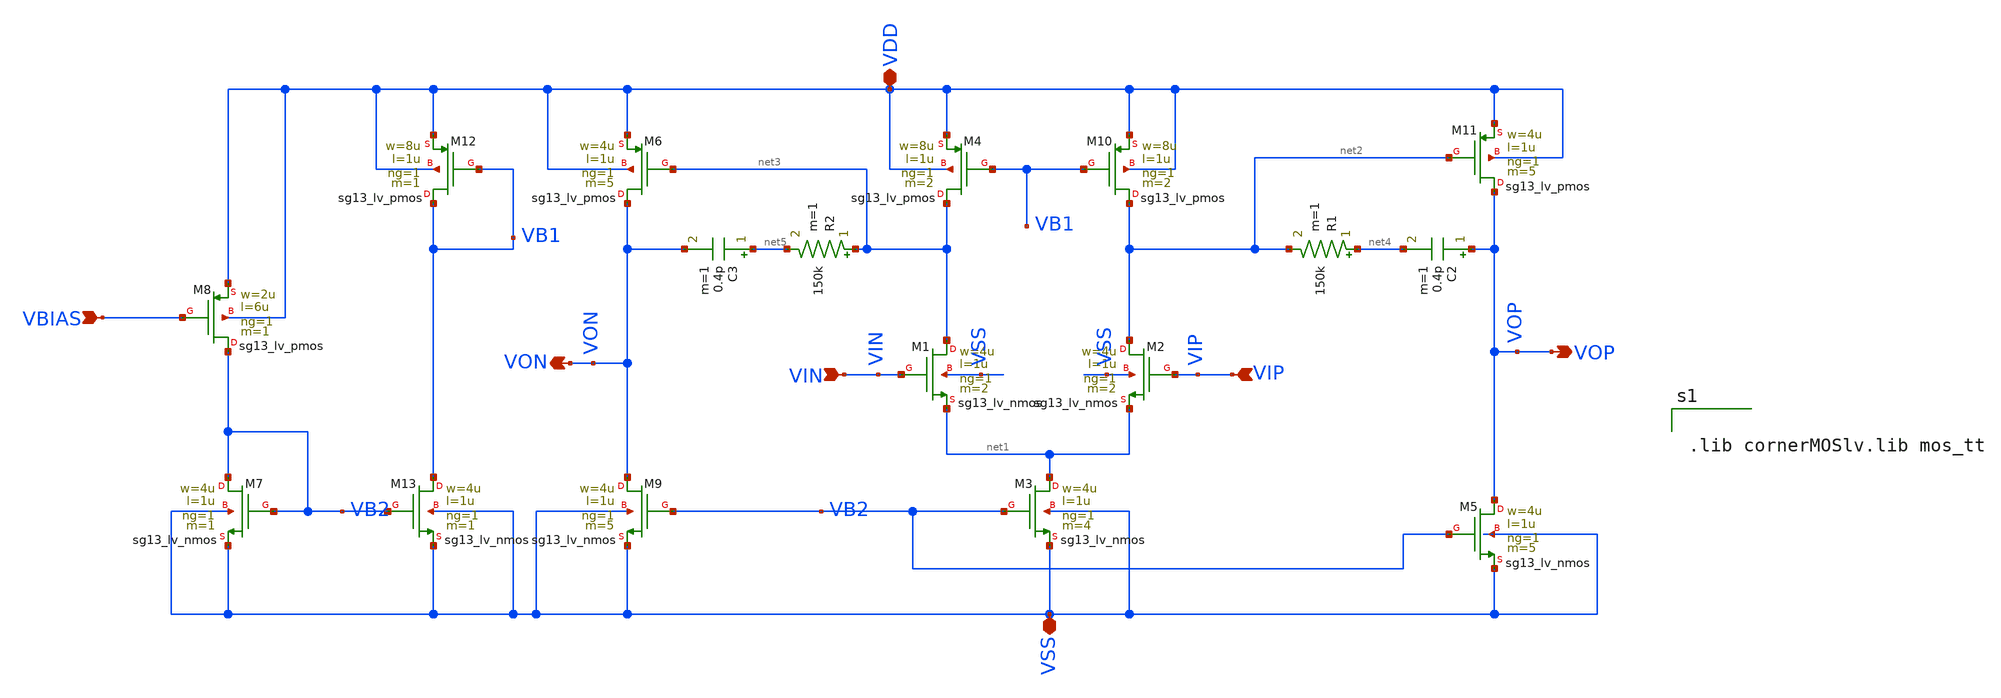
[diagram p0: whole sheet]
** sch_path: BTDay5-Ex/2-stage-opampCMFB.sch
**.subckt 2-stage-opampCMFB VIN VIP VOP VDD VSS VBIAS VON
*.ipin VIN
*.ipin VIP
*.opin VOP
*.iopin VDD
*.iopin VSS
*.ipin VBIAS
*.opin VON
XM1 net3 VIN net1 VSS sg13_lv_nmos w=4u l=1u ng=1 m=2 mm_ok=1
XM2 net2 VIP net1 VSS sg13_lv_nmos w=4u l=1u ng=1 m=2 mm_ok=1
XM3 net1 VB2 VSS VSS sg13_lv_nmos w=4u l=1u ng=1 m=4 mm_ok=1
XM4 net3 VB1 VDD VDD sg13_lv_pmos w=8u l=1u ng=1 m=2 mm_ok=1
XM7 VB2 VB2 VSS VSS sg13_lv_nmos w=4u l=1u ng=1 m=1 mm_ok=1
XM8 VB2 VBIAS VDD VDD sg13_lv_pmos w=2u l=6u ng=1 m=1 mm_ok=1
XM10 net2 VB1 VDD VDD sg13_lv_pmos w=8u l=1u ng=1 m=2 mm_ok=1
XM5 VOP VB2 VSS VSS sg13_lv_nmos w=4u l=1u ng=1 m=5 mm_ok=1
XM11 VOP net2 VDD VDD sg13_lv_pmos w=4u l=1u ng=1 m=5 mm_ok=1
C2 VOP net4 0.4p m=1
R1 net4 net2 150k m=1
XM9 VON VB2 VSS VSS sg13_lv_nmos w=4u l=1u ng=1 m=5 mm_ok=1
C3 net5 VON 0.4p m=1
R2 net3 net5 150k m=1
XM12 VB1 VB1 VDD VDD sg13_lv_pmos w=8u l=1u ng=1 m=1 mm_ok=1
XM13 VB1 VB2 VSS VSS sg13_lv_nmos w=4u l=1u ng=1 m=1 mm_ok=1
XM6 VON net3 VDD VDD sg13_lv_pmos w=4u l=1u ng=1 m=5 mm_ok=1
**** begin user architecture code


.lib cornerMOSlv.lib mos_tt




.control

*==================================================
* 1. SAVE OPERATING-POINT PARAMETERS
*==================================================

save all

* NMOS
save @n.xm1.nsg13_lv_nmos[ids] @n.xm1.nsg13_lv_nmos[vgs] @n.xm1.nsg13_lv_nmos[vth]
+ @n.xm1.nsg13_lv_nmos[vds] @n.xm1.nsg13_lv_nmos[vdss] @n.xm1.nsg13_lv_nmos[gm] @n.xm1.nsg13_lv_nmos[gds]

save @n.xm2.nsg13_lv_nmos[ids] @n.xm2.nsg13_lv_nmos[vgs] @n.xm2.nsg13_lv_nmos[vth]
+ @n.xm2.nsg13_lv_nmos[vds] @n.xm2.nsg13_lv_nmos[vdss] @n.xm2.nsg13_lv_nmos[gm] @n.xm2.nsg13_lv_nmos[gds]

save @n.xm3.nsg13_lv_nmos[ids] @n.xm3.nsg13_lv_nmos[vgs] @n.xm3.nsg13_lv_nmos[vth]
+ @n.xm3.nsg13_lv_nmos[vds] @n.xm3.nsg13_lv_nmos[vdss] @n.xm3.nsg13_lv_nmos[gm] @n.xm3.nsg13_lv_nmos[gds]

save @n.xm5.nsg13_lv_nmos[ids] @n.xm5.nsg13_lv_nmos[vgs] @n.xm5.nsg13_lv_nmos[vth]
+ @n.xm5.nsg13_lv_nmos[vds] @n.xm5.nsg13_lv_nmos[vdss] @n.xm5.nsg13_lv_nmos[gm] @n.xm5.nsg13_lv_nmos[gds]

save @n.xm7.nsg13_lv_nmos[ids] @n.xm7.nsg13_lv_nmos[vgs] @n.xm7.nsg13_lv_nmos[vth]
+ @n.xm7.nsg13_lv_nmos[vds] @n.xm7.nsg13_lv_nmos[vdss] @n.xm7.nsg13_lv_nmos[gm] @n.xm7.nsg13_lv_nmos[gds]

* PMOS
save @n.xm4.nsg13_lv_pmos[ids] @n.xm4.nsg13_lv_pmos[vgs] @n.xm4.nsg13_lv_pmos[vth]
+ @n.xm4.nsg13_lv_pmos[vds] @n.xm4.nsg13_lv_pmos[vdss] @n.xm4.nsg13_lv_pmos[gm] @n.xm4.nsg13_lv_pmos[gds]

save @n.xm8.nsg13_lv_pmos[ids] @n.xm8.nsg13_lv_pmos[vgs] @n.xm8.nsg13_lv_pmos[vth]
+ @n.xm8.nsg13_lv_pmos[vds] @n.xm8.nsg13_lv_pmos[vdss] @n.xm8.nsg13_lv_pmos[gm] @n.xm8.nsg13_lv_pmos[gds]

save @n.xm10.nsg13_lv_pmos[ids] @n.xm10.nsg13_lv_pmos[vgs] @n.xm10.nsg13_lv_pmos[vth]
+ @n.xm10.nsg13_lv_pmos[vds] @n.xm10.nsg13_lv_pmos[vdss] @n.xm10.nsg13_lv_pmos[gm] @n.xm10.nsg13_lv_pmos[gds]

save @n.xm11.nsg13_lv_pmos[ids] @n.xm11.nsg13_lv_pmos[vgs] @n.xm11.nsg13_lv_pmos[vth]
+ @n.xm11.nsg13_lv_pmos[vds] @n.xm11.nsg13_lv_pmos[vdss] @n.xm11.nsg13_lv_pmos[gm] @n.xm11.nsg13_lv_pmos[gds]


*==================================================
* 2. DC OPERATING POINT
*==================================================

op

echo ================= M1 NMOS =================
print @n.xm1.nsg13_lv_nmos[vgs] @n.xm1.nsg13_lv_nmos[vth] @n.xm1.nsg13_lv_nmos[vds]
+ @n.xm1.nsg13_lv_nmos[vdss] @n.xm1.nsg13_lv_nmos[ids] @n.xm1.nsg13_lv_nmos[gm] @n.xm1.nsg13_lv_nmos[gds]

echo ================= M2 NMOS =================
print @n.xm2.nsg13_lv_nmos[vgs] @n.xm2.nsg13_lv_nmos[vth] @n.xm2.nsg13_lv_nmos[vds]
+ @n.xm2.nsg13_lv_nmos[vdss] @n.xm2.nsg13_lv_nmos[ids] @n.xm2.nsg13_lv_nmos[gm] @n.xm2.nsg13_lv_nmos[gds]

echo ================= M3 NMOS =================
print @n.xm3.nsg13_lv_nmos[vgs] @n.xm3.nsg13_lv_nmos[vth] @n.xm3.nsg13_lv_nmos[vds]
+ @n.xm3.nsg13_lv_nmos[vdss] @n.xm3.nsg13_lv_nmos[ids] @n.xm3.nsg13_lv_nmos[gm] @n.xm3.nsg13_lv_nmos[gds]

echo ================= M5 NMOS =================
print @n.xm5.nsg13_lv_nmos[vgs] @n.xm5.nsg13_lv_nmos[vth] @n.xm5.nsg13_lv_nmos[vds]
+ @n.xm5.nsg13_lv_nmos[vdss] @n.xm5.nsg13_lv_nmos[ids] @n.xm5.nsg13_lv_nmos[gm] @n.xm5.nsg13_lv_nmos[gds]

echo ================= M7 NMOS =================
print @n.xm7.nsg13_lv_nmos[vgs] @n.xm7.nsg13_lv_nmos[vth] @n.xm7.nsg13_lv_nmos[vds]
+ @n.xm7.nsg13_lv_nmos[vdss] @n.xm7.nsg13_lv_nmos[ids] @n.xm7.nsg13_lv_nmos[gm] @n.xm7.nsg13_lv_nmos[gds]

echo ================= M4 PMOS =================
print @n.xm4.nsg13_lv_pmos[vgs] @n.xm4.nsg13_lv_pmos[vth] @n.xm4.nsg13_lv_pmos[vds]
+ @n.xm4.nsg13_lv_pmos[vdss] @n.xm4.nsg13_lv_pmos[ids] @n.xm4.nsg13_lv_pmos[gm] @n.xm4.nsg13_lv_pmos[gds]

echo ================= M8 PMOS =================
print @n.xm8.nsg13_lv_pmos[vgs] @n.xm8.nsg13_lv_pmos[vth] @n.xm8.nsg13_lv_pmos[vds]
+ @n.xm8.nsg13_lv_pmos[vdss] @n.xm8.nsg13_lv_pmos[ids] @n.xm8.nsg13_lv_pmos[gm] @n.xm8.nsg13_lv_pmos[gds]

echo ================= M10 PMOS ================
print @n.xm10.nsg13_lv_pmos[vgs] @n.xm10.nsg13_lv_pmos[vth] @n.xm10.nsg13_lv_pmos[vds]
+ @n.xm10.nsg13_lv_pmos[vdss] @n.xm10.nsg13_lv_pmos[ids] @n.xm10.nsg13_lv_pmos[gm] @n.xm10.nsg13_lv_pmos[gds]

echo ================= M11 PMOS ================
print @n.xm11.nsg13_lv_pmos[vgs] @n.xm11.nsg13_lv_pmos[vth] @n.xm11.nsg13_lv_pmos[vds]
+ @n.xm11.nsg13_lv_pmos[vdss] @n.xm11.nsg13_lv_pmos[ids] @n.xm11.nsg13_lv_pmos[gm] @n.xm11.nsg13_lv_pmos[gds]

print v(vop) v(von)
print v(vg11) v(vg6)
print v(vb1) v(vb2)


write op_operating_point.raw

*==================================================
* 3. DIFFERENTIAL AC GAIN AND PHASE
*==================================================

ac dec 200 1 10G

let vid = v(vip)-v(vin)
let vod = v(vop)-v(von)
let av_diff = vod/vid

let gain_db = db(av_diff)
let phase_deg = cph(av_diff)*180/pi

if phase_deg[0] > 90
    let phase_deg = phase_deg-360
end

plot gain_db phase_deg xlog ylimit -360 80 title Differential

**** end user architecture code
**.ends
.end
